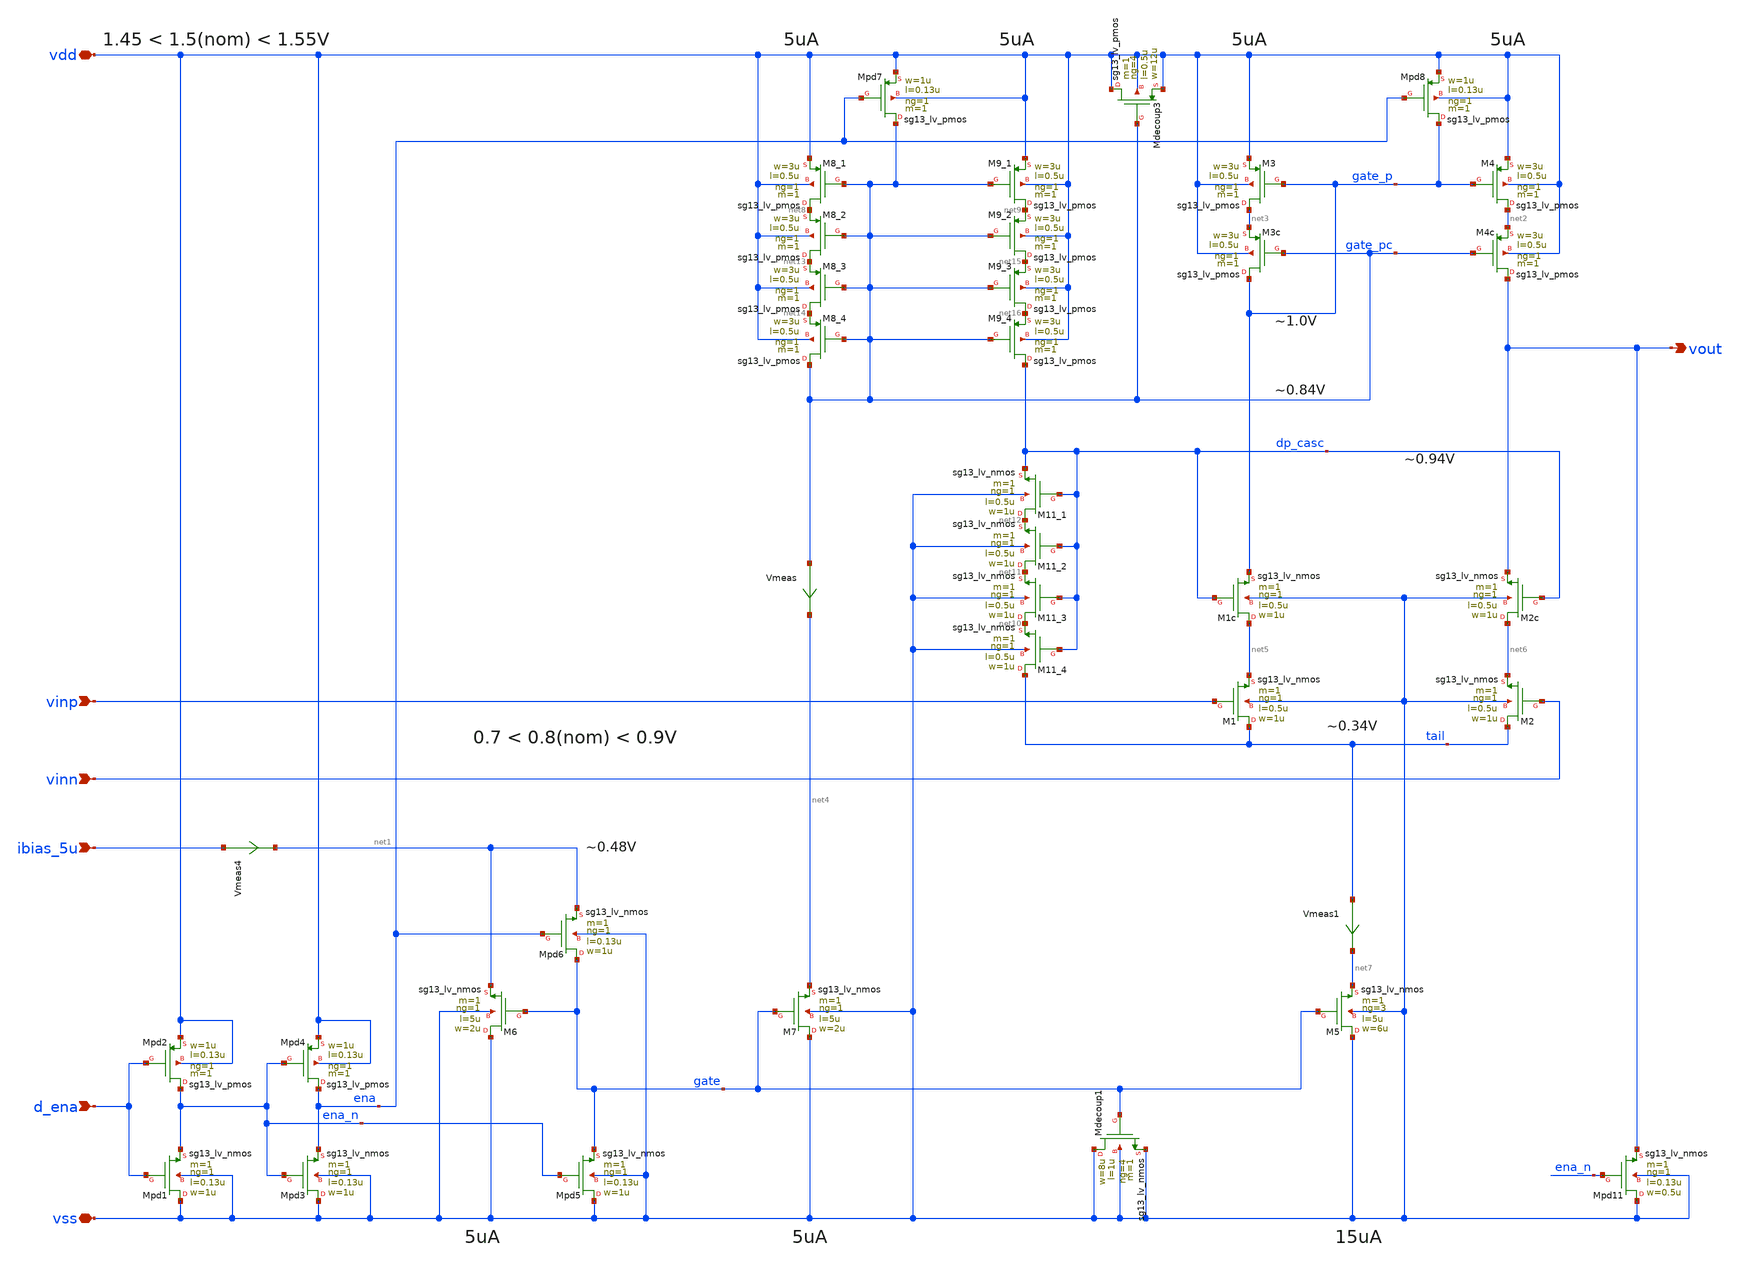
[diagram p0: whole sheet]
** sch_path: xschem/ota-improved.sch
* (c) 2024 H. Pretl, Apache-2.0 license
**.subckt ota-improved ibias_5u vdd vss vinp vinn vout d_ena
*.ipin ibias_5u
*.iopin vdd
*.iopin vss
*.ipin vinp
*.ipin vinn
*.opin vout
*.ipin d_ena
XM5 vss gate net7 vss sg13_lv_nmos w=6u l=5u ng=3 m=1 mm_ok=1
XM4 net2 gate_p vdd vdd sg13_lv_pmos w=3u l=0.5u ng=1 m=1 mm_ok=1
XM1 tail vinp net5 vss sg13_lv_nmos w=1u l=0.5u ng=1 m=1 mm_ok=1
XM2 tail vinn net6 vss sg13_lv_nmos w=1u l=0.5u ng=1 m=1 mm_ok=1
XM3 net3 gate_p vdd vdd sg13_lv_pmos w=3u l=0.5u ng=1 m=1 mm_ok=1
XM6 vss gate net1 vss sg13_lv_nmos w=2u l=5u ng=1 m=1 mm_ok=1
XMpd5 vss ena_n gate vss sg13_lv_nmos w=1u l=0.13u ng=1 m=1 mm_ok=1
XMpd3 vss ena_n ena vss sg13_lv_nmos w=1u l=0.13u ng=1 m=1 mm_ok=1
XMpd4 ena ena_n vdd vdd sg13_lv_pmos w=1u l=0.13u ng=1 m=1 mm_ok=1
XMpd6 gate ena net1 vss sg13_lv_nmos w=1u l=0.13u ng=1 m=1 mm_ok=1
XM2c net6 dp_casc vout vss sg13_lv_nmos w=1u l=0.5u ng=1 m=1 mm_ok=1
XM1c net5 dp_casc gate_p vss sg13_lv_nmos w=1u l=0.5u ng=1 m=1 mm_ok=1
XM4c vout gate_pc net2 vdd sg13_lv_pmos w=3u l=0.5u ng=1 m=1 mm_ok=1
XM3c gate_p gate_pc net3 vdd sg13_lv_pmos w=3u l=0.5u ng=1 m=1 mm_ok=1
XM7 vss gate net4 vss sg13_lv_nmos w=2u l=5u ng=1 m=1 mm_ok=1
XMpd8 gate_p ena vdd vdd sg13_lv_pmos w=1u l=0.13u ng=1 m=1 mm_ok=1
XM8_1 net8 gate_pc vdd vdd sg13_lv_pmos w=3u l=0.5u ng=1 m=1 mm_ok=1
XM9_1 net9 gate_pc vdd vdd sg13_lv_pmos w=3u l=0.5u ng=1 m=1 mm_ok=1
XMpd7 gate_pc ena vdd vdd sg13_lv_pmos w=1u l=0.13u ng=1 m=1 mm_ok=1
XM11_3 net10 dp_casc net11 vss sg13_lv_nmos w=1u l=0.5u ng=1 m=1 mm_ok=1
Vmeas gate_pc net4 0
.save i(vmeas)
Vmeas1 tail net7 0
.save i(vmeas1)
XMpd1 vss d_ena ena_n vss sg13_lv_nmos w=1u l=0.13u ng=1 m=1 mm_ok=1
XMpd2 ena_n d_ena vdd vdd sg13_lv_pmos w=1u l=0.13u ng=1 m=1 mm_ok=1
Vmeas4 ibias_5u net1 0
.save i(vmeas4)
XMpd11 vss ena_n vout vss sg13_lv_nmos w=0.5u l=0.13u ng=1 m=1 mm_ok=1
XM11_4 tail dp_casc net10 vss sg13_lv_nmos w=1u l=0.5u ng=1 m=1 mm_ok=1
XMdecoup1 vss gate vss vss sg13_lv_nmos w=8u l=1u ng=4 m=1 mm_ok=1
XMdecoup3 vdd gate_pc vdd vdd sg13_lv_pmos w=12u l=0.5u ng=4 m=1 mm_ok=1
XM11_2 net11 dp_casc net12 vss sg13_lv_nmos w=1u l=0.5u ng=1 m=1 mm_ok=1
XM11_1 net12 dp_casc dp_casc vss sg13_lv_nmos w=1u l=0.5u ng=1 m=1 mm_ok=1
XM8_2 net13 gate_pc net8 vdd sg13_lv_pmos w=3u l=0.5u ng=1 m=1 mm_ok=1
XM8_3 net14 gate_pc net13 vdd sg13_lv_pmos w=3u l=0.5u ng=1 m=1 mm_ok=1
XM9_2 net15 gate_pc net9 vdd sg13_lv_pmos w=3u l=0.5u ng=1 m=1 mm_ok=1
XM9_3 net16 gate_pc net15 vdd sg13_lv_pmos w=3u l=0.5u ng=1 m=1 mm_ok=1
XM8_4 gate_pc gate_pc net14 vdd sg13_lv_pmos w=3u l=0.5u ng=1 m=1 mm_ok=1
XM9_4 dp_casc gate_pc net16 vdd sg13_lv_pmos w=3u l=0.5u ng=1 m=1 mm_ok=1
**.ends
.end
